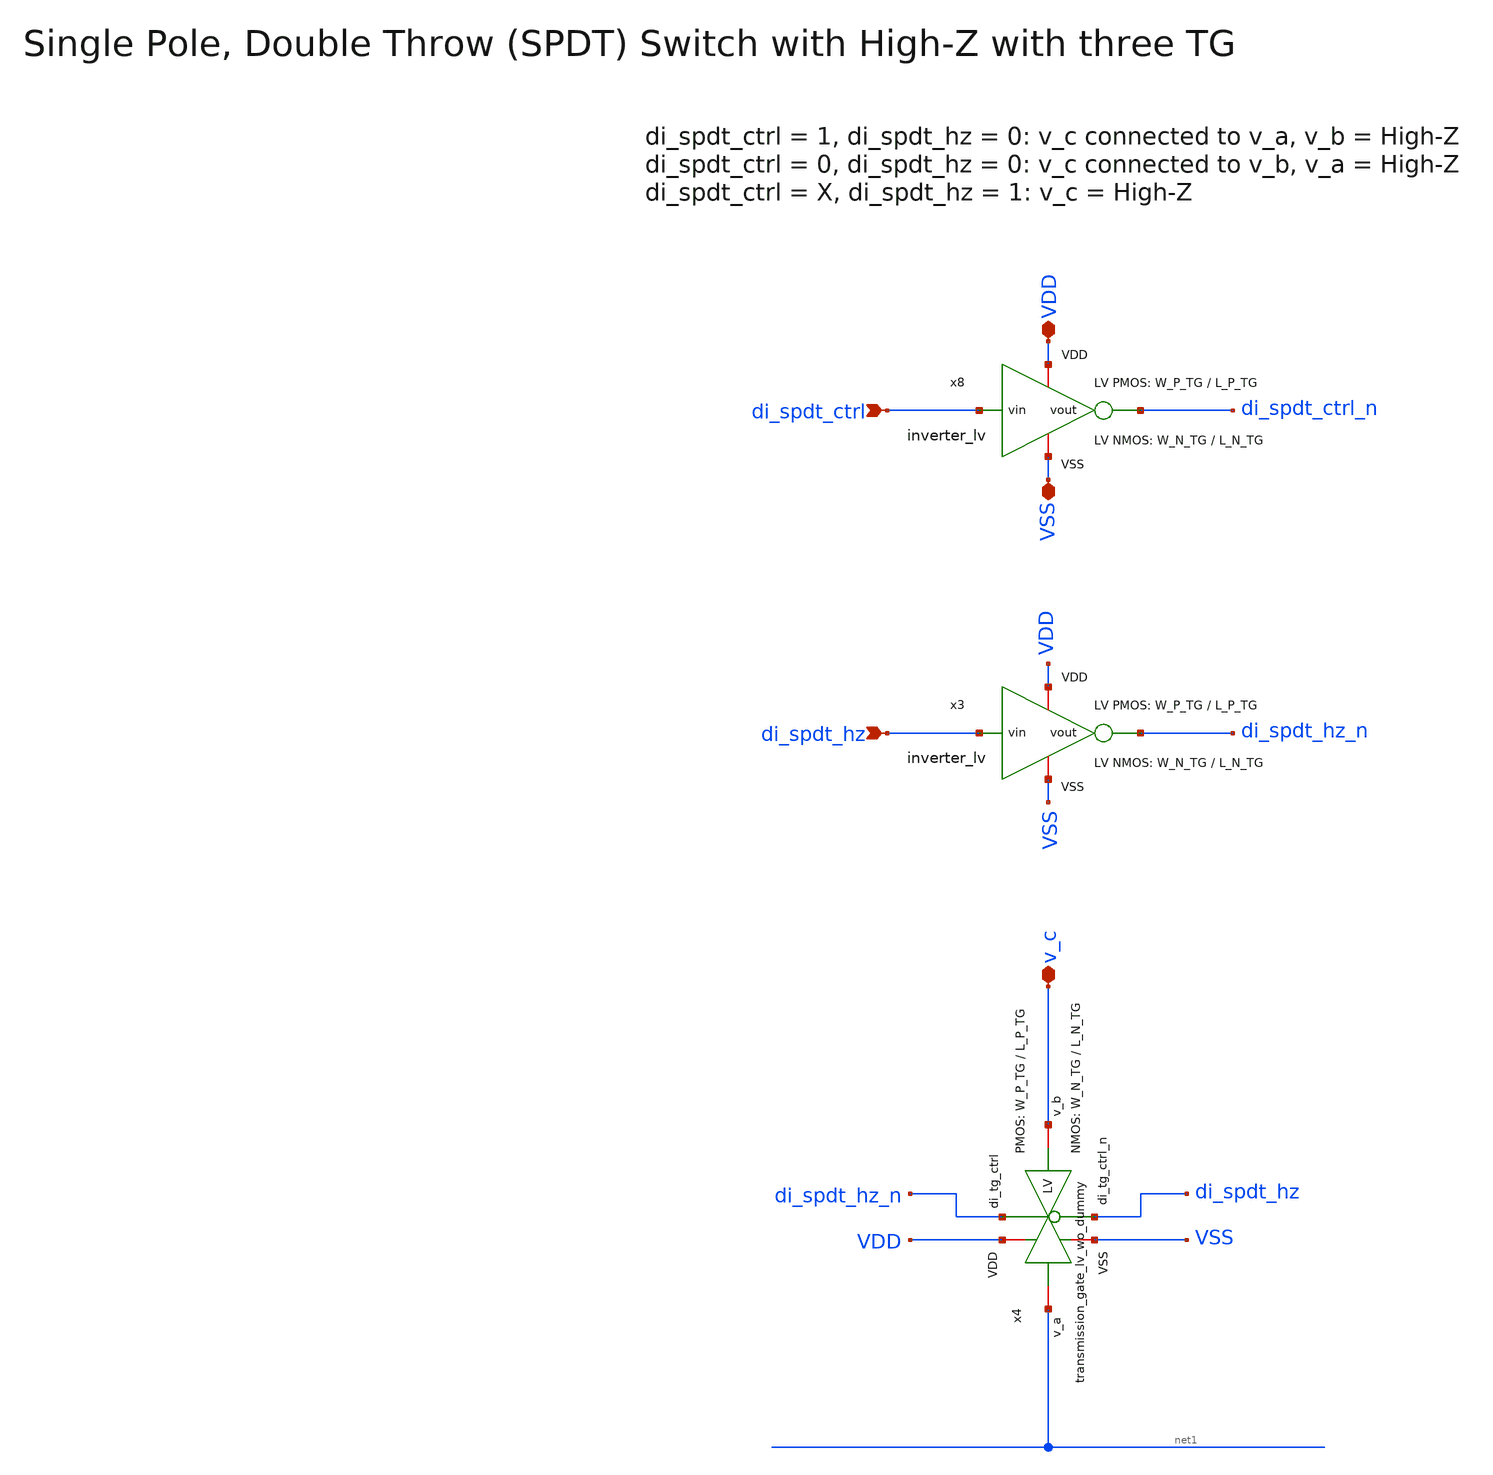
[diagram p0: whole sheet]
** sch_path: xschem/spdt_switch/spdt_hz_switch.sch
**.subckt spdt_hz_switch v_c VDD VSS di_spdt_ctrl di_spdt_hz
*.iopin v_c
*.iopin VDD
*.iopin VSS
*.ipin di_spdt_ctrl
*.ipin di_spdt_hz
x8 VDD di_spdt_ctrl di_spdt_ctrl_n VSS inverter_lv W_P=W_P_TG L_P=L_P_TG W_N=W_N_TG L_N=L_N_TG n=1
x3 VDD di_spdt_hz di_spdt_hz_n VSS inverter_lv W_P=W_P_TG L_P=L_P_TG W_N=W_N_TG L_N=L_N_TG n=1
x4 VDD di_spdt_hz_n VSS v_c net1 di_spdt_hz transmission_gate_lv_wo_dummy W_P=W_P_TG L_P=L_P_TG
+ W_N=W_N_TG L_N=L_N_TG W_P_D=1.0u L_P_D=0.13u W_N_D=1.0u L_N_D=0.13u n=1
**.ends

* expanding   symbol:  inverter/inverter_lv.sym # of pins=4
** sym_path: xschem/inverter/inverter_lv.sym
** sch_path: xschem/inverter/inverter_lv.sch
.subckt inverter_lv VDD vin vout VSS  W_P=3.0u L_P=0.13u W_N=1.0u L_N=0.13u n=1
*.ipin vin
*.iopin VDD
*.iopin VSS
*.opin vout
XM1 vout vin VDD VDD sg13_lv_pmos w=W_P l=L_P ng=1 m=n mm_ok=1
XM2 vout vin VSS VSS sg13_lv_nmos w=W_N l=L_N ng=1 m=n mm_ok=1
.ends


* expanding   symbol:  transmission_gate/transmission_gate_lv_wo_dummy.sym # of pins=6
** sym_path: xschem/transmission_gate/transmission_gate_lv_wo_dummy.sym
** sch_path: xschem/transmission_gate/transmission_gate_lv_wo_dummy.sch
.subckt transmission_gate_lv_wo_dummy VDD di_tg_ctrl VSS v_b v_a di_tg_ctrl_n  W_P=2.0u L_P=0.13u
+ W_N=2.0u L_N=0.13u W_P_D=1.0u L_P_D=0.13u W_N_D=1.0u L_N_D=0.13u n=1
*.iopin v_a
*.iopin v_b
*.iopin VDD
*.iopin VSS
*.ipin di_tg_ctrl
*.ipin di_tg_ctrl_n
XM1 v_a di_tg_ctrl v_b VSS sg13_lv_nmos w=W_N l=L_N ng=1 m=n mm_ok=1
XM2 v_a di_tg_ctrl_n v_b VDD sg13_lv_pmos w=W_P l=L_P ng=1 m=n mm_ok=1
.ends

.end
